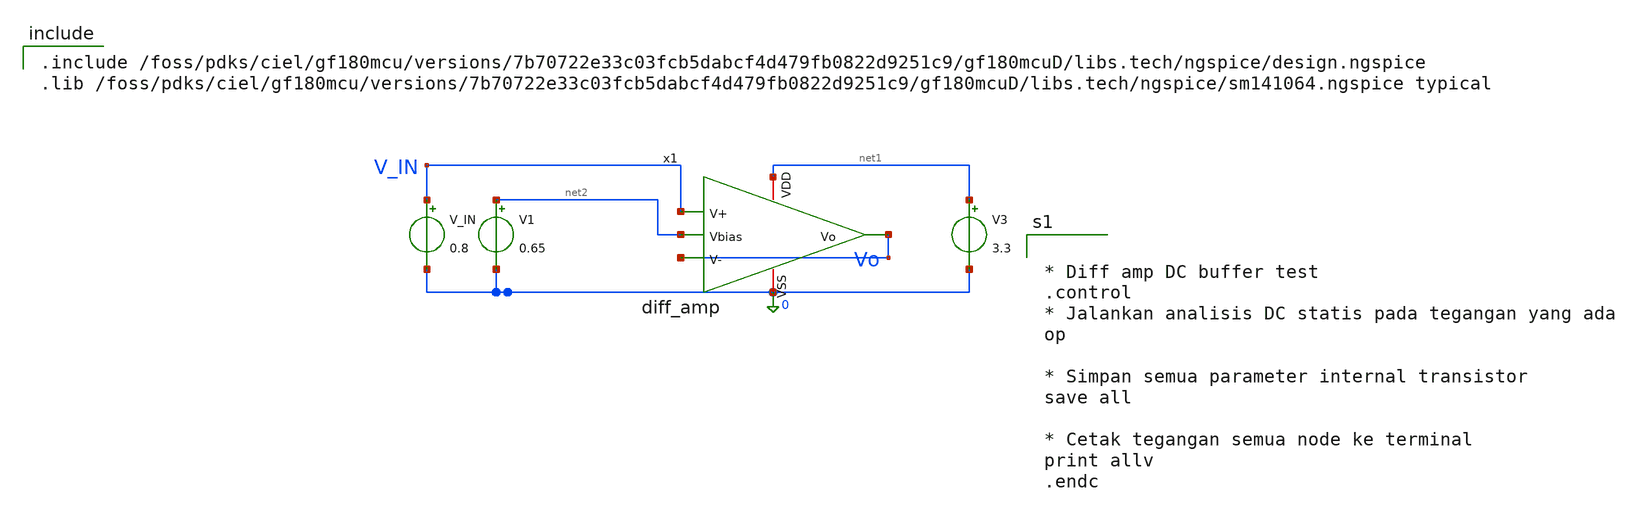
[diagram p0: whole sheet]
** sch_path: analog/tb_diff_amp.sch
**.subckt tb_diff_amp
x1 net1 Vo V_IN Vo net2 0 diff_amp
V1 net2 0 0.65
V_IN V_IN 0 0.8
V3 net1 0 3.3
**** begin user architecture code

.include /foss/pdks/ciel/gf180mcu/versions/7b70722e33c03fcb5dabcf4d479fb0822d9251c9/gf180mcuD/libs.tech/ngspice/design.ngspice
.lib /foss/pdks/ciel/gf180mcu/versions/7b70722e33c03fcb5dabcf4d479fb0822d9251c9/gf180mcuD/libs.tech/ngspice/sm141064.ngspice typical



* Diff amp DC buffer test
.control
* Jalankan analisis DC statis pada tegangan yang ada
op

* Simpan semua parameter internal transistor
save all

* Cetak tegangan semua node ke terminal
print allv
.endc


**** end user architecture code
**.ends

* expanding   symbol:
*+  AURA-Event-Driven-Mixed-Signal-ASIC-for-Acoustic-Pattern-Detection/analog/diff_amp.sym # of pins=6
** sym_path: analog/diff_amp.sym
** sch_path: analog/diff_amp.sch
.subckt diff_amp VDD Vo V+ V- Vbias VSS
*.iopin VDD
*.iopin VSS
*.ipin V+
*.ipin V-
*.opin Vo
*.ipin Vbias
XM1 net1 V+ net2 VSS nfet_03v3 L=0.28u W=0.22u nf=1 ad='int((nf+1)/2) * W/nf * 0.18u' as='int((nf+2)/2) * W/nf * 0.18u'
+ pd='2*int((nf+1)/2) * (W/nf + 0.18u)' ps='2*int((nf+2)/2) * (W/nf + 0.18u)' nrd='0.18u / W' nrs='0.18u / W'
+ sa=0 sb=0 sd=0 m=1
XM2 net2 Vbias VSS VSS nfet_03v3 L=0.28u W=0.22u nf=1 ad='int((nf+1)/2) * W/nf * 0.18u' as='int((nf+2)/2) * W/nf * 0.18u'
+ pd='2*int((nf+1)/2) * (W/nf + 0.18u)' ps='2*int((nf+2)/2) * (W/nf + 0.18u)' nrd='0.18u / W' nrs='0.18u / W'
+ sa=0 sb=0 sd=0 m=1
XM3 Vo V- net2 VSS nfet_03v3 L=0.28u W=0.22u nf=1 ad='int((nf+1)/2) * W/nf * 0.18u' as='int((nf+2)/2) * W/nf * 0.18u'
+ pd='2*int((nf+1)/2) * (W/nf + 0.18u)' ps='2*int((nf+2)/2) * (W/nf + 0.18u)' nrd='0.18u / W' nrs='0.18u / W'
+ sa=0 sb=0 sd=0 m=1
XM4 Vo net1 VDD VDD pfet_03v3 L=0.28u W=0.22u nf=1 ad='int((nf+1)/2) * W/nf * 0.18u' as='int((nf+2)/2) * W/nf * 0.18u'
+ pd='2*int((nf+1)/2) * (W/nf + 0.18u)' ps='2*int((nf+2)/2) * (W/nf + 0.18u)' nrd='0.18u / W' nrs='0.18u / W'
+ sa=0 sb=0 sd=0 m=1
XM5 net1 net1 VDD VDD pfet_03v3 L=0.28u W=0.22u nf=1 ad='int((nf+1)/2) * W/nf * 0.18u' as='int((nf+2)/2) * W/nf * 0.18u'
+ pd='2*int((nf+1)/2) * (W/nf + 0.18u)' ps='2*int((nf+2)/2) * (W/nf + 0.18u)' nrd='0.18u / W' nrs='0.18u / W'
+ sa=0 sb=0 sd=0 m=1
.ends

.end
